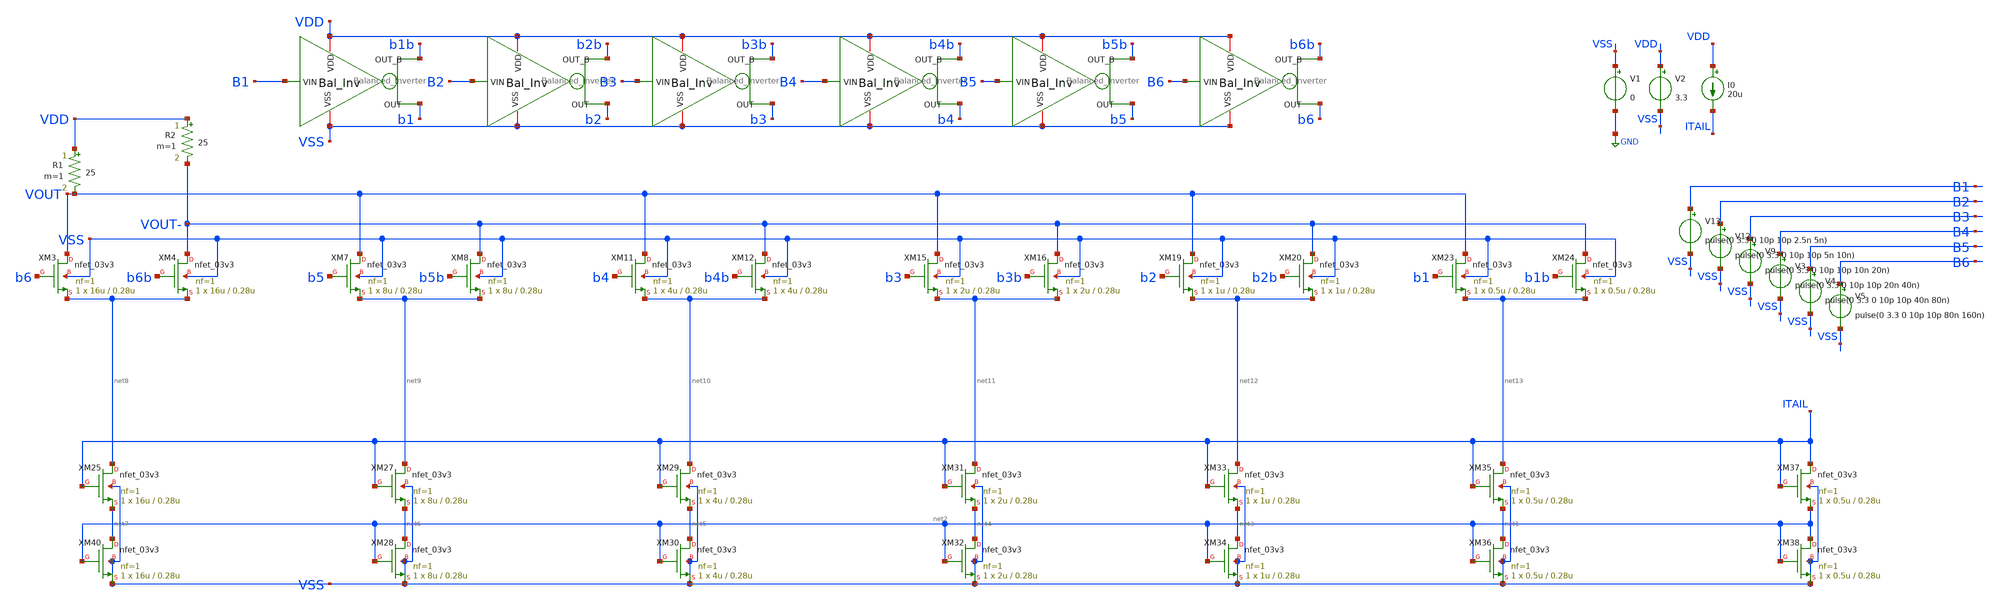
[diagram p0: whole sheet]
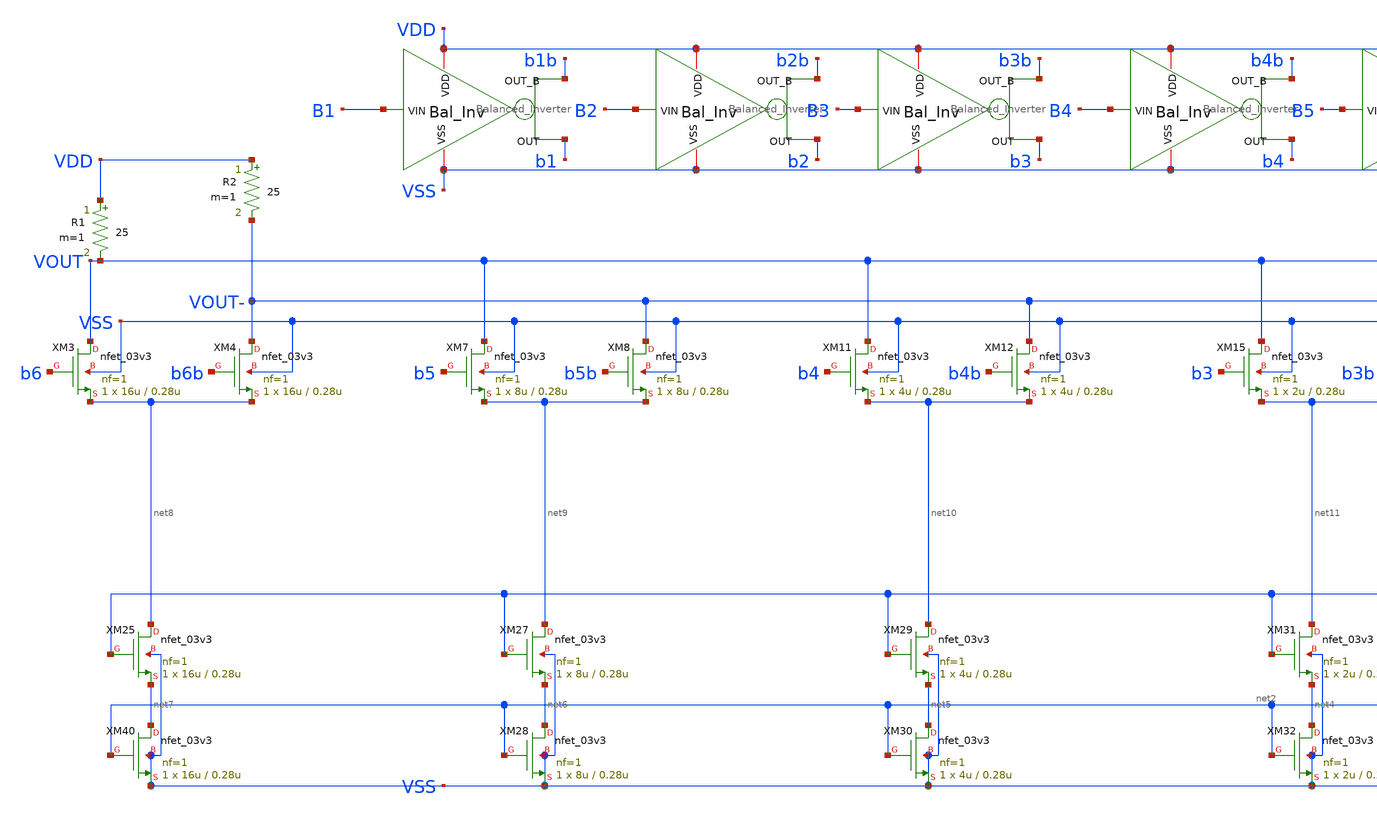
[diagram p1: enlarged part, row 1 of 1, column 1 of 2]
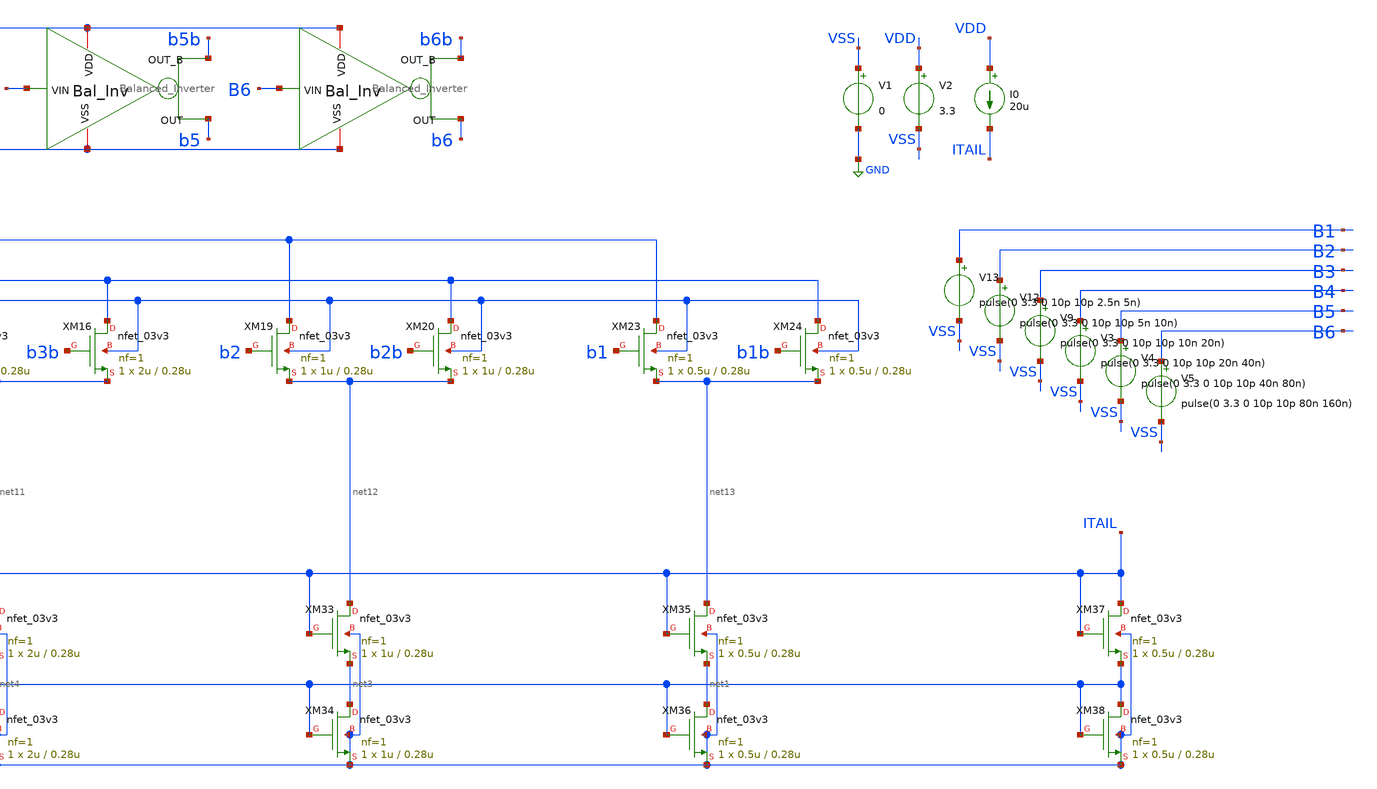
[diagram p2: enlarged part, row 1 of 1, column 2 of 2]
** sch_path: DAC_PAKISTAN_01/Pakistan1_Xschem/DAC_conv.sch
**.subckt DAC_conv
x1 VDD VSS B1 b1b b1 Balanced_Inverter
x2 VDD VSS B2 b2b b2 Balanced_Inverter
x3 VDD VSS B3 b3b b3 Balanced_Inverter
x4 VDD VSS B4 b4b b4 Balanced_Inverter
x5 VDD VSS B5 b5b b5 Balanced_Inverter
x6 VDD VSS B6 b6b b6 Balanced_Inverter
XM3 VOUT b6 net8 VSS nfet_03v3 L=0.28u W=16u nf=1 ad='int((nf+1)/2) * W/nf * 0.18u' as='int((nf+2)/2) * W/nf * 0.18u'
+ pd='2*int((nf+1)/2) * (W/nf + 0.18u)' ps='2*int((nf+2)/2) * (W/nf + 0.18u)' nrd='0.18u / W' nrs='0.18u / W'
+ sa=0 sb=0 sd=0 m=1
XM4 VOUT- b6b net8 VSS nfet_03v3 L=0.28u W=16u nf=1 ad='int((nf+1)/2) * W/nf * 0.18u' as='int((nf+2)/2) * W/nf * 0.18u'
+ pd='2*int((nf+1)/2) * (W/nf + 0.18u)' ps='2*int((nf+2)/2) * (W/nf + 0.18u)' nrd='0.18u / W' nrs='0.18u / W'
+ sa=0 sb=0 sd=0 m=1
XM7 VOUT b5 net9 VSS nfet_03v3 L=0.28u W=8u nf=1 ad='int((nf+1)/2) * W/nf * 0.18u' as='int((nf+2)/2) * W/nf * 0.18u'
+ pd='2*int((nf+1)/2) * (W/nf + 0.18u)' ps='2*int((nf+2)/2) * (W/nf + 0.18u)' nrd='0.18u / W' nrs='0.18u / W'
+ sa=0 sb=0 sd=0 m=1
XM8 VOUT- b5b net9 VSS nfet_03v3 L=0.28u W=8u nf=1 ad='int((nf+1)/2) * W/nf * 0.18u' as='int((nf+2)/2) * W/nf * 0.18u'
+ pd='2*int((nf+1)/2) * (W/nf + 0.18u)' ps='2*int((nf+2)/2) * (W/nf + 0.18u)' nrd='0.18u / W' nrs='0.18u / W'
+ sa=0 sb=0 sd=0 m=1
XM11 VOUT b4 net10 VSS nfet_03v3 L=0.28u W=4u nf=1 ad='int((nf+1)/2) * W/nf * 0.18u' as='int((nf+2)/2) * W/nf * 0.18u'
+ pd='2*int((nf+1)/2) * (W/nf + 0.18u)' ps='2*int((nf+2)/2) * (W/nf + 0.18u)' nrd='0.18u / W' nrs='0.18u / W'
+ sa=0 sb=0 sd=0 m=1
XM12 VOUT- b4b net10 VSS nfet_03v3 L=0.28u W=4u nf=1 ad='int((nf+1)/2) * W/nf * 0.18u' as='int((nf+2)/2) * W/nf * 0.18u'
+ pd='2*int((nf+1)/2) * (W/nf + 0.18u)' ps='2*int((nf+2)/2) * (W/nf + 0.18u)' nrd='0.18u / W' nrs='0.18u / W'
+ sa=0 sb=0 sd=0 m=1
XM15 VOUT b3 net11 VSS nfet_03v3 L=0.28u W=2u nf=1 ad='int((nf+1)/2) * W/nf * 0.18u' as='int((nf+2)/2) * W/nf * 0.18u'
+ pd='2*int((nf+1)/2) * (W/nf + 0.18u)' ps='2*int((nf+2)/2) * (W/nf + 0.18u)' nrd='0.18u / W' nrs='0.18u / W'
+ sa=0 sb=0 sd=0 m=1
XM16 VOUT- b3b net11 VSS nfet_03v3 L=0.28u W=2u nf=1 ad='int((nf+1)/2) * W/nf * 0.18u' as='int((nf+2)/2) * W/nf * 0.18u'
+ pd='2*int((nf+1)/2) * (W/nf + 0.18u)' ps='2*int((nf+2)/2) * (W/nf + 0.18u)' nrd='0.18u / W' nrs='0.18u / W'
+ sa=0 sb=0 sd=0 m=1
XM19 VOUT b2 net12 VSS nfet_03v3 L=0.28u W=1u nf=1 ad='int((nf+1)/2) * W/nf * 0.18u' as='int((nf+2)/2) * W/nf * 0.18u'
+ pd='2*int((nf+1)/2) * (W/nf + 0.18u)' ps='2*int((nf+2)/2) * (W/nf + 0.18u)' nrd='0.18u / W' nrs='0.18u / W'
+ sa=0 sb=0 sd=0 m=1
XM20 VOUT- b2b net12 VSS nfet_03v3 L=0.28u W=1u nf=1 ad='int((nf+1)/2) * W/nf * 0.18u' as='int((nf+2)/2) * W/nf * 0.18u'
+ pd='2*int((nf+1)/2) * (W/nf + 0.18u)' ps='2*int((nf+2)/2) * (W/nf + 0.18u)' nrd='0.18u / W' nrs='0.18u / W'
+ sa=0 sb=0 sd=0 m=1
XM23 VOUT b1 net13 VSS nfet_03v3 L=0.28u W=0.5u nf=1 ad='int((nf+1)/2) * W/nf * 0.18u' as='int((nf+2)/2) * W/nf * 0.18u'
+ pd='2*int((nf+1)/2) * (W/nf + 0.18u)' ps='2*int((nf+2)/2) * (W/nf + 0.18u)' nrd='0.18u / W' nrs='0.18u / W'
+ sa=0 sb=0 sd=0 m=1
XM24 VOUT- b1b net13 VSS nfet_03v3 L=0.28u W=0.5u nf=1 ad='int((nf+1)/2) * W/nf * 0.18u' as='int((nf+2)/2) * W/nf * 0.18u'
+ pd='2*int((nf+1)/2) * (W/nf + 0.18u)' ps='2*int((nf+2)/2) * (W/nf + 0.18u)' nrd='0.18u / W' nrs='0.18u / W'
+ sa=0 sb=0 sd=0 m=1
XM25 net8 ITAIL net7 VSS nfet_03v3 L=0.28u W=16u nf=1 ad='int((nf+1)/2) * W/nf * 0.18u' as='int((nf+2)/2) * W/nf * 0.18u'
+ pd='2*int((nf+1)/2) * (W/nf + 0.18u)' ps='2*int((nf+2)/2) * (W/nf + 0.18u)' nrd='0.18u / W' nrs='0.18u / W'
+ sa=0 sb=0 sd=0 m=1
XM27 net9 ITAIL net6 VSS nfet_03v3 L=0.28u W=8u nf=1 ad='int((nf+1)/2) * W/nf * 0.18u' as='int((nf+2)/2) * W/nf * 0.18u'
+ pd='2*int((nf+1)/2) * (W/nf + 0.18u)' ps='2*int((nf+2)/2) * (W/nf + 0.18u)' nrd='0.18u / W' nrs='0.18u / W'
+ sa=0 sb=0 sd=0 m=1
XM28 net6 net2 VSS VSS nfet_03v3 L=0.28u W=8u nf=1 ad='int((nf+1)/2) * W/nf * 0.18u' as='int((nf+2)/2) * W/nf * 0.18u'
+ pd='2*int((nf+1)/2) * (W/nf + 0.18u)' ps='2*int((nf+2)/2) * (W/nf + 0.18u)' nrd='0.18u / W' nrs='0.18u / W'
+ sa=0 sb=0 sd=0 m=1
XM29 net10 ITAIL net5 VSS nfet_03v3 L=0.28u W=4u nf=1 ad='int((nf+1)/2) * W/nf * 0.18u' as='int((nf+2)/2) * W/nf * 0.18u'
+ pd='2*int((nf+1)/2) * (W/nf + 0.18u)' ps='2*int((nf+2)/2) * (W/nf + 0.18u)' nrd='0.18u / W' nrs='0.18u / W'
+ sa=0 sb=0 sd=0 m=1
XM30 net5 net2 VSS VSS nfet_03v3 L=0.28u W=4u nf=1 ad='int((nf+1)/2) * W/nf * 0.18u' as='int((nf+2)/2) * W/nf * 0.18u'
+ pd='2*int((nf+1)/2) * (W/nf + 0.18u)' ps='2*int((nf+2)/2) * (W/nf + 0.18u)' nrd='0.18u / W' nrs='0.18u / W'
+ sa=0 sb=0 sd=0 m=1
XM31 net11 ITAIL net4 VSS nfet_03v3 L=0.28u W=2u nf=1 ad='int((nf+1)/2) * W/nf * 0.18u' as='int((nf+2)/2) * W/nf * 0.18u'
+ pd='2*int((nf+1)/2) * (W/nf + 0.18u)' ps='2*int((nf+2)/2) * (W/nf + 0.18u)' nrd='0.18u / W' nrs='0.18u / W'
+ sa=0 sb=0 sd=0 m=1
XM32 net4 net2 VSS VSS nfet_03v3 L=0.28u W=2u nf=1 ad='int((nf+1)/2) * W/nf * 0.18u' as='int((nf+2)/2) * W/nf * 0.18u'
+ pd='2*int((nf+1)/2) * (W/nf + 0.18u)' ps='2*int((nf+2)/2) * (W/nf + 0.18u)' nrd='0.18u / W' nrs='0.18u / W'
+ sa=0 sb=0 sd=0 m=1
XM33 net12 ITAIL net3 VSS nfet_03v3 L=0.28u W=1u nf=1 ad='int((nf+1)/2) * W/nf * 0.18u' as='int((nf+2)/2) * W/nf * 0.18u'
+ pd='2*int((nf+1)/2) * (W/nf + 0.18u)' ps='2*int((nf+2)/2) * (W/nf + 0.18u)' nrd='0.18u / W' nrs='0.18u / W'
+ sa=0 sb=0 sd=0 m=1
XM34 net3 net2 VSS VSS nfet_03v3 L=0.28u W=1u nf=1 ad='int((nf+1)/2) * W/nf * 0.18u' as='int((nf+2)/2) * W/nf * 0.18u'
+ pd='2*int((nf+1)/2) * (W/nf + 0.18u)' ps='2*int((nf+2)/2) * (W/nf + 0.18u)' nrd='0.18u / W' nrs='0.18u / W'
+ sa=0 sb=0 sd=0 m=1
XM35 net13 ITAIL net1 VSS nfet_03v3 L=0.28u W=0.5u nf=1 ad='int((nf+1)/2) * W/nf * 0.18u' as='int((nf+2)/2) * W/nf * 0.18u'
+ pd='2*int((nf+1)/2) * (W/nf + 0.18u)' ps='2*int((nf+2)/2) * (W/nf + 0.18u)' nrd='0.18u / W' nrs='0.18u / W'
+ sa=0 sb=0 sd=0 m=1
XM36 net1 net2 VSS VSS nfet_03v3 L=0.28u W=0.5u nf=1 ad='int((nf+1)/2) * W/nf * 0.18u' as='int((nf+2)/2) * W/nf * 0.18u'
+ pd='2*int((nf+1)/2) * (W/nf + 0.18u)' ps='2*int((nf+2)/2) * (W/nf + 0.18u)' nrd='0.18u / W' nrs='0.18u / W'
+ sa=0 sb=0 sd=0 m=1
XM37 ITAIL ITAIL net2 VSS nfet_03v3 L=0.28u W=0.5u nf=1 ad='int((nf+1)/2) * W/nf * 0.18u' as='int((nf+2)/2) * W/nf * 0.18u'
+ pd='2*int((nf+1)/2) * (W/nf + 0.18u)' ps='2*int((nf+2)/2) * (W/nf + 0.18u)' nrd='0.18u / W' nrs='0.18u / W'
+ sa=0 sb=0 sd=0 m=1
XM38 net2 net2 VSS VSS nfet_03v3 L=0.28u W=0.5u nf=1 ad='int((nf+1)/2) * W/nf * 0.18u' as='int((nf+2)/2) * W/nf * 0.18u'
+ pd='2*int((nf+1)/2) * (W/nf + 0.18u)' ps='2*int((nf+2)/2) * (W/nf + 0.18u)' nrd='0.18u / W' nrs='0.18u / W'
+ sa=0 sb=0 sd=0 m=1
XM40 net7 net2 VSS VSS nfet_03v3 L=0.28u W=16u nf=1 ad='int((nf+1)/2) * W/nf * 0.18u' as='int((nf+2)/2) * W/nf * 0.18u'
+ pd='2*int((nf+1)/2) * (W/nf + 0.18u)' ps='2*int((nf+2)/2) * (W/nf + 0.18u)' nrd='0.18u / W' nrs='0.18u / W'
+ sa=0 sb=0 sd=0 m=1
R1 VDD VOUT 25 m=1
R2 VDD VOUT- 25 m=1
V1 VSS GND 0
V2 VDD VSS 3.3
I0 VDD ITAIL 20u
V3 B4 VSS pulse(0 3.3 0 10p 10p 20n 40n)
V4 B5 VSS pulse(0 3.3 0 10p 10p 40n 80n)
V5 B6 VSS pulse(0 3.3 0 10p 10p 80n 160n)
V9 B3 VSS pulse(0 3.3 0 10p 10p 10n 20n)
V12 B2 VSS pulse(0 3.3 0 10p 10p 5n 10n)
V13 B1 VSS pulse(0 3.3 0 10p 10p 2.5n 5n)
**** begin user architecture code

.include $::180MCU_MODELS/design.ngspice
.lib $::180MCU_MODELS/sm141064.ngspice typical




.control
save all
op

tran 10p 200n
plot v(VOUT)
*write test_nfet_03v3.raw
.endc


**** end user architecture code
**.ends

* expanding   symbol:  Balanced_Inverter.sym # of pins=5
** sym_path: DAC_PAKISTAN_01/Pakistan1_Xschem/Balanced_Inverter.sym
** sch_path: DAC_PAKISTAN_01/Pakistan1_Xschem/Balanced_Inverter.sch
.subckt Balanced_Inverter VDD VSS VIN OUT_B OUT
*.iopin VSS
*.ipin VIN
*.opin OUT_B
*.iopin VDD
*.opin OUT
XM1 OUT_B VIN VSS VSS nfet_03v3 L=0.28u W=0.22u nf=1 ad='int((nf+1)/2) * W/nf * 0.18u' as='int((nf+2)/2) * W/nf * 0.18u'
+ pd='2*int((nf+1)/2) * (W/nf + 0.18u)' ps='2*int((nf+2)/2) * (W/nf + 0.18u)' nrd='0.18u / W' nrs='0.18u / W'
+ sa=0 sb=0 sd=0 m=1
XM2 OUT_B OUT VDD VDD pfet_03v3 L=0.28u W=0.22u nf=1 ad='int((nf+1)/2) * W/nf * 0.18u' as='int((nf+2)/2) * W/nf * 0.18u'
+ pd='2*int((nf+1)/2) * (W/nf + 0.18u)' ps='2*int((nf+2)/2) * (W/nf + 0.18u)' nrd='0.18u / W' nrs='0.18u / W'
+ sa=0 sb=0 sd=0 m=1
XM3 OUT net1 VSS VSS nfet_03v3 L=0.28u W=0.22u nf=1 ad='int((nf+1)/2) * W/nf * 0.18u' as='int((nf+2)/2) * W/nf * 0.18u'
+ pd='2*int((nf+1)/2) * (W/nf + 0.18u)' ps='2*int((nf+2)/2) * (W/nf + 0.18u)' nrd='0.18u / W' nrs='0.18u / W'
+ sa=0 sb=0 sd=0 m=1
XM4 OUT OUT_B VDD VDD pfet_03v3 L=0.28u W=0.22u nf=1 ad='int((nf+1)/2) * W/nf * 0.18u' as='int((nf+2)/2) * W/nf * 0.18u'
+ pd='2*int((nf+1)/2) * (W/nf + 0.18u)' ps='2*int((nf+2)/2) * (W/nf + 0.18u)' nrd='0.18u / W' nrs='0.18u / W'
+ sa=0 sb=0 sd=0 m=1
x1 VSS VDD net1 VIN GF_INV
.ends


* expanding   symbol:  GF_INV.sym # of pins=4
** sym_path: GF_INV.sym
** sch_path: GF_INV.sch
.subckt GF_INV VSS VDD OUT IN
*.iopin VDD
*.iopin VSS
*.ipin IN
*.opin OUT
XM1 OUT IN VSS VSS nfet_03v3 L=0.28u W=0.25u nf=1 ad='int((nf+1)/2) * W/nf * 0.18u' as='int((nf+2)/2) * W/nf * 0.18u'
+ pd='2*int((nf+1)/2) * (W/nf + 0.18u)' ps='2*int((nf+2)/2) * (W/nf + 0.18u)' nrd='0.18u / W' nrs='0.18u / W'
+ sa=0 sb=0 sd=0 m=1
XM2 OUT IN VDD VDD pfet_03v3 L=0.28u W=0.5u nf=1 ad='int((nf+1)/2) * W/nf * 0.18u' as='int((nf+2)/2) * W/nf * 0.18u'
+ pd='2*int((nf+1)/2) * (W/nf + 0.18u)' ps='2*int((nf+2)/2) * (W/nf + 0.18u)' nrd='0.18u / W' nrs='0.18u / W'
+ sa=0 sb=0 sd=0 m=1
.ends

.GLOBAL GND
.end
